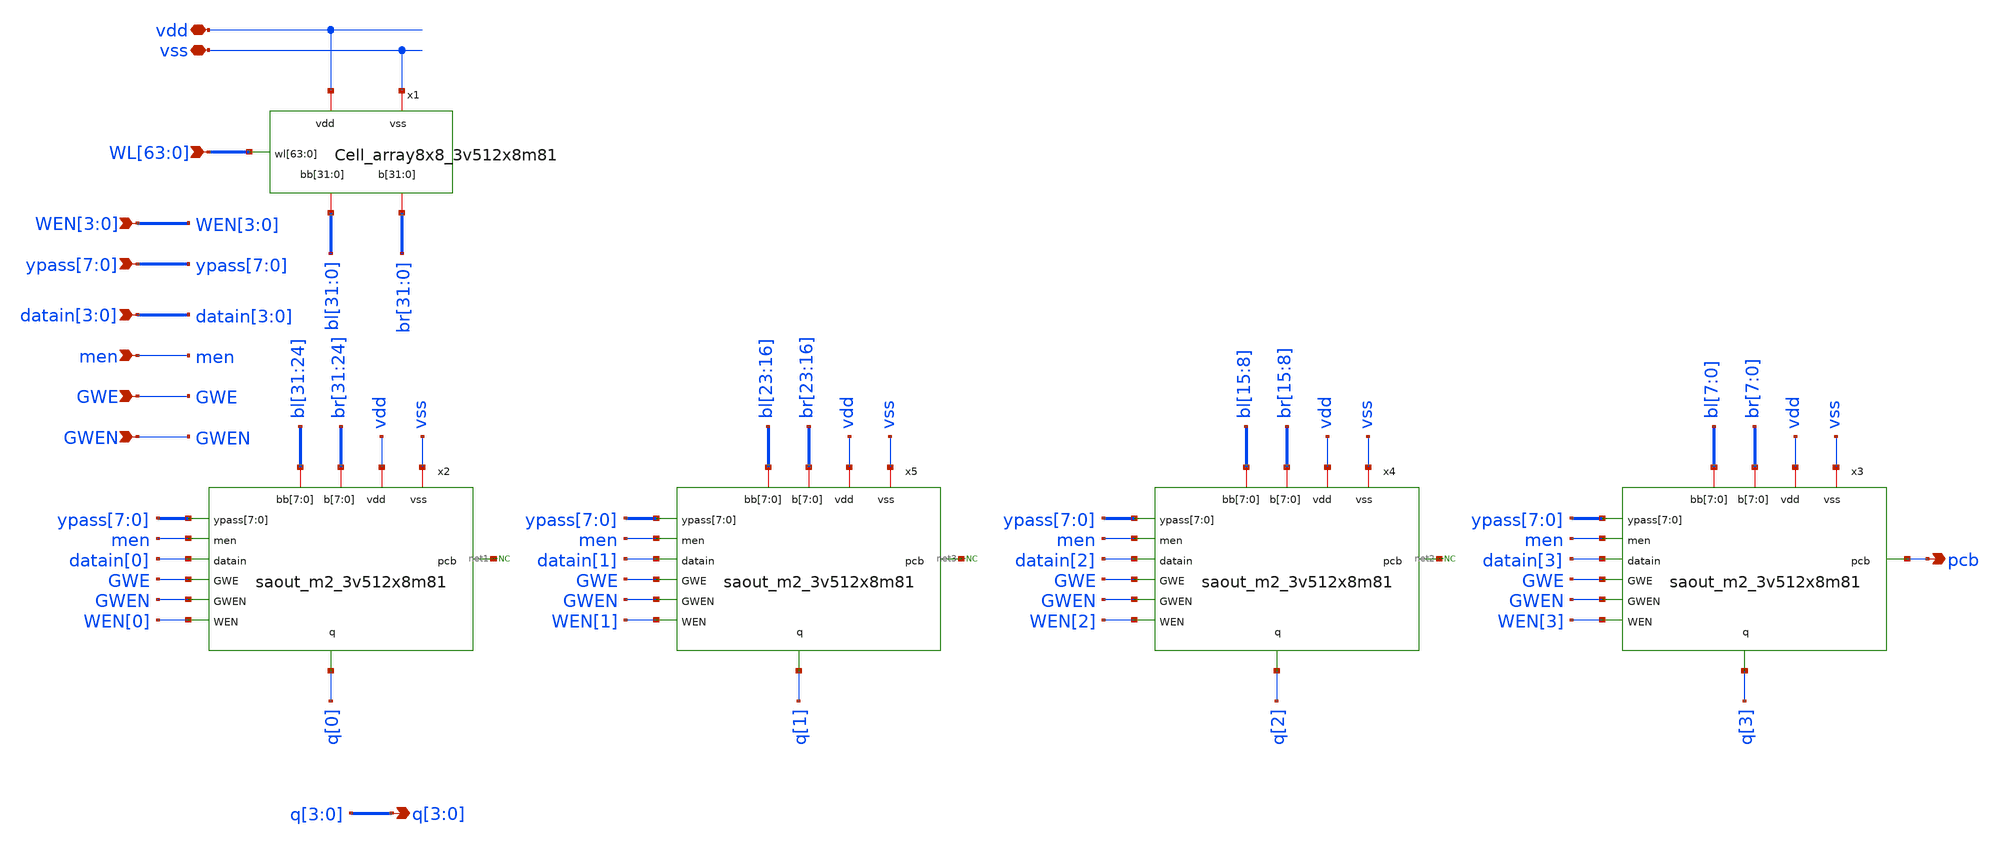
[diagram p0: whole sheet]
** sch_path: cells/gf180mcu_ocd_ip_sram__sram512x8m8wm1/xschem/col_512a_3v512x8m81.sch
**.subckt col_512a_3v512x8m81
*+ WL[63],WL[62],WL[61],WL[60],WL[59],WL[58],WL[57],WL[56],WL[55],WL[54],WL[53],WL[52],WL[51],WL[50],WL[49],WL[48],WL[47],WL[46],WL[45],WL[44],WL[43],WL[42],WL[41],WL[40],WL[39],WL[38],WL[37],WL[36],WL[35],WL[34],WL[33],WL[32],WL[31],WL[30],WL[29],WL[28],WL[27],WL[26],WL[25],WL[24],WL[23],WL[22],WL[21],WL[20],WL[19],WL[18],WL[17],WL[16],WL[15],WL[14],WL[13],WL[12],WL[11],WL[10],WL[9],WL[8],WL[7],WL[6],WL[5],WL[4],WL[3],WL[2],WL[1],WL[0] vdd vss WEN[3],WEN[2],WEN[1],WEN[0] q[3],q[2],q[1],q[0]
*+ ypass[7],ypass[6],ypass[5],ypass[4],ypass[3],ypass[2],ypass[1],ypass[0] datain[3],datain[2],datain[1],datain[0] men GWE GWEN pcb
*.ipin
*+ WL[63],WL[62],WL[61],WL[60],WL[59],WL[58],WL[57],WL[56],WL[55],WL[54],WL[53],WL[52],WL[51],WL[50],WL[49],WL[48],WL[47],WL[46],WL[45],WL[44],WL[43],WL[42],WL[41],WL[40],WL[39],WL[38],WL[37],WL[36],WL[35],WL[34],WL[33],WL[32],WL[31],WL[30],WL[29],WL[28],WL[27],WL[26],WL[25],WL[24],WL[23],WL[22],WL[21],WL[20],WL[19],WL[18],WL[17],WL[16],WL[15],WL[14],WL[13],WL[12],WL[11],WL[10],WL[9],WL[8],WL[7],WL[6],WL[5],WL[4],WL[3],WL[2],WL[1],WL[0]
*.iopin vdd
*.iopin vss
*.ipin WEN[3],WEN[2],WEN[1],WEN[0]
*.opin q[3],q[2],q[1],q[0]
*.ipin ypass[7],ypass[6],ypass[5],ypass[4],ypass[3],ypass[2],ypass[1],ypass[0]
*.ipin datain[3],datain[2],datain[1],datain[0]
*.ipin men
*.ipin GWE
*.ipin GWEN
*.opin pcb
x1 WL[63] WL[62] WL[61] WL[60] WL[59] WL[58] WL[57] WL[56] WL[55] WL[54] WL[53] WL[52] WL[51] WL[50]
+ WL[49] WL[48] WL[47] WL[46] WL[45] WL[44] WL[43] WL[42] WL[41] WL[40] WL[39] WL[38] WL[37] WL[36] WL[35]
+ WL[34] WL[33] WL[32] WL[31] WL[30] WL[29] WL[28] WL[27] WL[26] WL[25] WL[24] WL[23] WL[22] WL[21] WL[20]
+ WL[19] WL[18] WL[17] WL[16] WL[15] WL[14] WL[13] WL[12] WL[11] WL[10] WL[9] WL[8] WL[7] WL[6] WL[5] WL[4]
+ WL[3] WL[2] WL[1] WL[0] bl[31] bl[30] bl[29] bl[28] bl[27] bl[26] bl[25] bl[24] bl[23] bl[22] bl[21]
+ bl[20] bl[19] bl[18] bl[17] bl[16] bl[15] bl[14] bl[13] bl[12] bl[11] bl[10] bl[9] bl[8] bl[7] bl[6] bl[5]
+ bl[4] bl[3] bl[2] bl[1] bl[0] br[31] br[30] br[29] br[28] br[27] br[26] br[25] br[24] br[23] br[22]
+ br[21] br[20] br[19] br[18] br[17] br[16] br[15] br[14] br[13] br[12] br[11] br[10] br[9] br[8] br[7]
+ br[6] br[5] br[4] br[3] br[2] br[1] br[0] vdd vss Cell_array8x8_3v512x8m81
x2 vdd vss bl[31] bl[30] bl[29] bl[28] bl[27] bl[26] bl[25] bl[24] br[31] br[30] br[29] br[28]
+ br[27] br[26] br[25] br[24] ypass[7] ypass[6] ypass[5] ypass[4] ypass[3] ypass[2] ypass[1] ypass[0] men
+ datain[0] GWE q[0] GWEN WEN[0] net1 saout_m2_3v512x8m81
x4 vdd vss bl[15] bl[14] bl[13] bl[12] bl[11] bl[10] bl[9] bl[8] br[15] br[14] br[13] br[12] br[11]
+ br[10] br[9] br[8] ypass[7] ypass[6] ypass[5] ypass[4] ypass[3] ypass[2] ypass[1] ypass[0] men datain[2]
+ GWE q[2] GWEN WEN[2] net2 saout_m2_3v512x8m81
* noconn #net1
* noconn #net3
* noconn #net2
x3 vdd vss bl[7] bl[6] bl[5] bl[4] bl[3] bl[2] bl[1] bl[0] br[7] br[6] br[5] br[4] br[3] br[2] br[1]
+ br[0] ypass[7] ypass[6] ypass[5] ypass[4] ypass[3] ypass[2] ypass[1] ypass[0] men datain[3] GWE q[3] GWEN
+ WEN[3] pcb saout_m2_3v512x8m81
x5 vdd vss bl[23] bl[22] bl[21] bl[20] bl[19] bl[18] bl[17] bl[16] br[23] br[22] br[21] br[20]
+ br[19] br[18] br[17] br[16] ypass[7] ypass[6] ypass[5] ypass[4] ypass[3] ypass[2] ypass[1] ypass[0] men
+ datain[1] GWE q[1] GWEN WEN[1] net3 saout_m2_3v512x8m81
**.ends
.end
